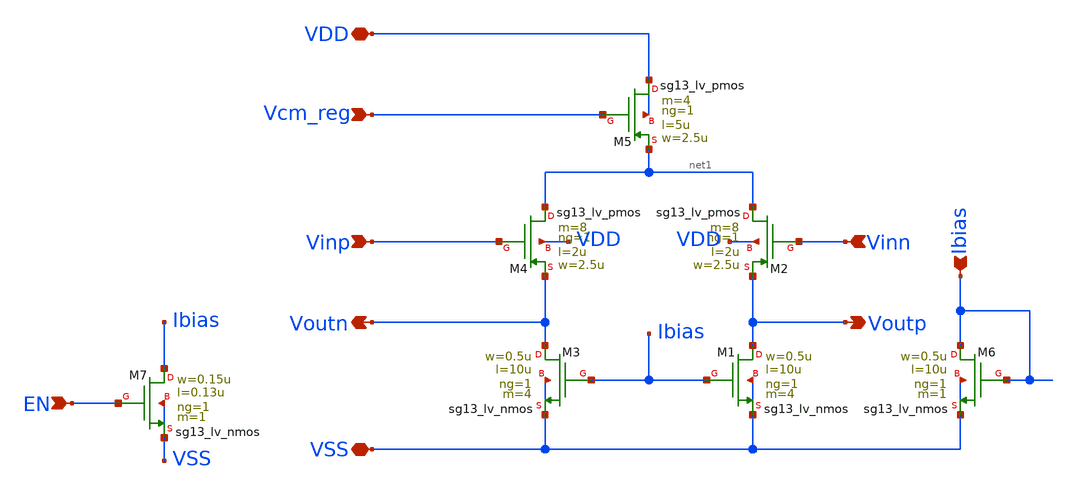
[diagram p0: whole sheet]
** sch_path: schema/ota_cmfb_core/ota_cmfb_core.sch
**.subckt ota_cmfb_core Voutn Voutp VDD VSS Vinp Ibias Vinn Vcm_reg EN
*.opin Voutn
*.opin Voutp
*.iopin VDD
*.iopin VSS
*.ipin Vinp
*.ipin Ibias
*.ipin Vinn
*.ipin Vcm_reg
*.ipin EN
XM1 Voutp Ibias VSS VSS sg13_lv_nmos w=0.5u l=10u ng=1 m=4 mm_ok=1
XM2 net1 Vinn Voutp VDD sg13_lv_pmos w=2.5u l=2u ng=1 m=8 mm_ok=1
XM3 Voutn Ibias VSS VSS sg13_lv_nmos w=0.5u l=10u ng=1 m=4 mm_ok=1
XM4 net1 Vinp Voutn VDD sg13_lv_pmos w=2.5u l=2u ng=1 m=8 mm_ok=1
XM5 VDD Vcm_reg net1 VDD sg13_lv_pmos w=2.5u l=5u ng=1 m=4 mm_ok=1
XM6 Ibias Ibias VSS VSS sg13_lv_nmos w=0.5u l=10u ng=1 m=1 mm_ok=1
XM7 Ibias EN VSS VSS sg13_lv_nmos w=0.15u l=0.13u ng=1 m=1 mm_ok=1
**.ends
.end
